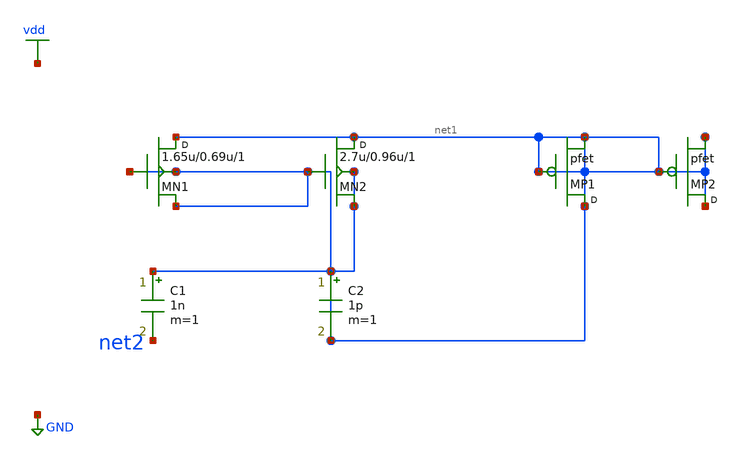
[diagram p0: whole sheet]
** sch_path: synthetic/generated/0022_synthetic.sch
**.subckt 0022_synthetic
MN1 net1 net1 net1 net1 nfet w=1.65u l=0.69u m=1
MN2 net1 net1 net1 net1 nfet w=2.7u l=0.96u m=1
MP1 net1 net1 net1 pfet m=1
MP2 net1 net1 net1 pfet m=1
C1 net1 net2 1n m=1
C2 net1 net1 1p m=1
**.ends
.GLOBAL vdd
.GLOBAL GND
.end
